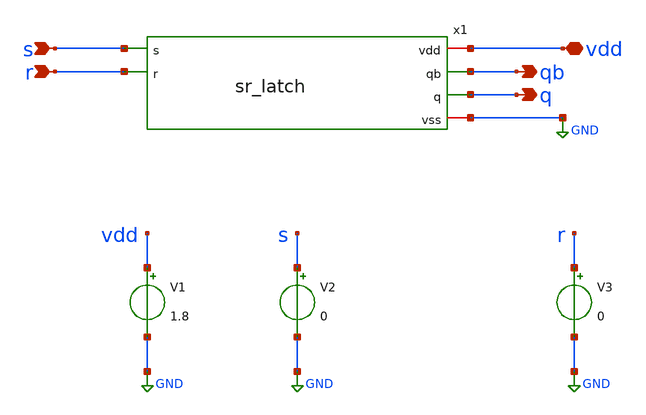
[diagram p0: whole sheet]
** sch_path: xschem/sr_latch_tbh.sch
**.subckt sr_latch_tbh s r vdd q qb
*.ipin s
*.ipin r
*.iopin vdd
*.opin q
*.opin qb
x1 vdd s qb q GND r sr_latch
V1 vdd GND 1.8
V2 s GND 0
V3 r GND 0
**** begin user architecture code

** opencircuitdesign pdks install
.lib $::SKYWATER_MODELS/sky130.lib.spice tt



* .options filetype=ascii

.control

tran 0.1n 200n
plot v(s)
plot v(r)
plot v(q)
plot v(qb)
*write ring_osc.raw
.endc
.end


**** end user architecture code
**.ends

* expanding   symbol:  sr_latch.sym # of pins=6
** sym_path: xschem/sr_latch.sym
** sch_path: xschem/sr_latch.sch
.subckt sr_latch vdd s qb q vss r
*.ipin s
*.ipin r
*.opin qb
*.opin q
*.iopin vss
*.iopin vdd
x1 vdd s q qb vss nor_gate
x2 vdd q qb r vss nor_gate
.ends


* expanding   symbol:  nor_gate.sym # of pins=5
** sym_path: xschem/nor_gate.sym
** sch_path: xschem/nor_gate.sch
.subckt nor_gate vdd a y b vss
*.ipin a
*.ipin b
*.opin y
*.iopin vdd
*.iopin vss
XM1 net1 a vdd vdd sky130_fd_pr__pfet_01v8 L=0.15 W=1.5 nf=1 ad='int((nf+1)/2) * W/nf * 0.29' as='int((nf+2)/2) * W/nf * 0.29'
+ pd='2*int((nf+1)/2) * (W/nf + 0.29)' ps='2*int((nf+2)/2) * (W/nf + 0.29)' nrd='0.29 / W' nrs='0.29 / W'
+ sa=0 sb=0 sd=0 mult=1 m=1
XM2 y b net1 vdd sky130_fd_pr__pfet_01v8 L=0.15 W=1.5 nf=1 ad='int((nf+1)/2) * W/nf * 0.29' as='int((nf+2)/2) * W/nf * 0.29'
+ pd='2*int((nf+1)/2) * (W/nf + 0.29)' ps='2*int((nf+2)/2) * (W/nf + 0.29)' nrd='0.29 / W' nrs='0.29 / W'
+ sa=0 sb=0 sd=0 mult=1 m=1
XM3 y a vss vss sky130_fd_pr__nfet_01v8 L=0.15 W=0.75 nf=1 ad='int((nf+1)/2) * W/nf * 0.29' as='int((nf+2)/2) * W/nf * 0.29'
+ pd='2*int((nf+1)/2) * (W/nf + 0.29)' ps='2*int((nf+2)/2) * (W/nf + 0.29)' nrd='0.29 / W' nrs='0.29 / W'
+ sa=0 sb=0 sd=0 mult=1 m=1
XM4 y b vss vss sky130_fd_pr__nfet_01v8 L=0.15 W=0.75 nf=1 ad='int((nf+1)/2) * W/nf * 0.29' as='int((nf+2)/2) * W/nf * 0.29'
+ pd='2*int((nf+1)/2) * (W/nf + 0.29)' ps='2*int((nf+2)/2) * (W/nf + 0.29)' nrd='0.29 / W' nrs='0.29 / W'
+ sa=0 sb=0 sd=0 mult=1 m=1
.ends

.GLOBAL GND
.end
